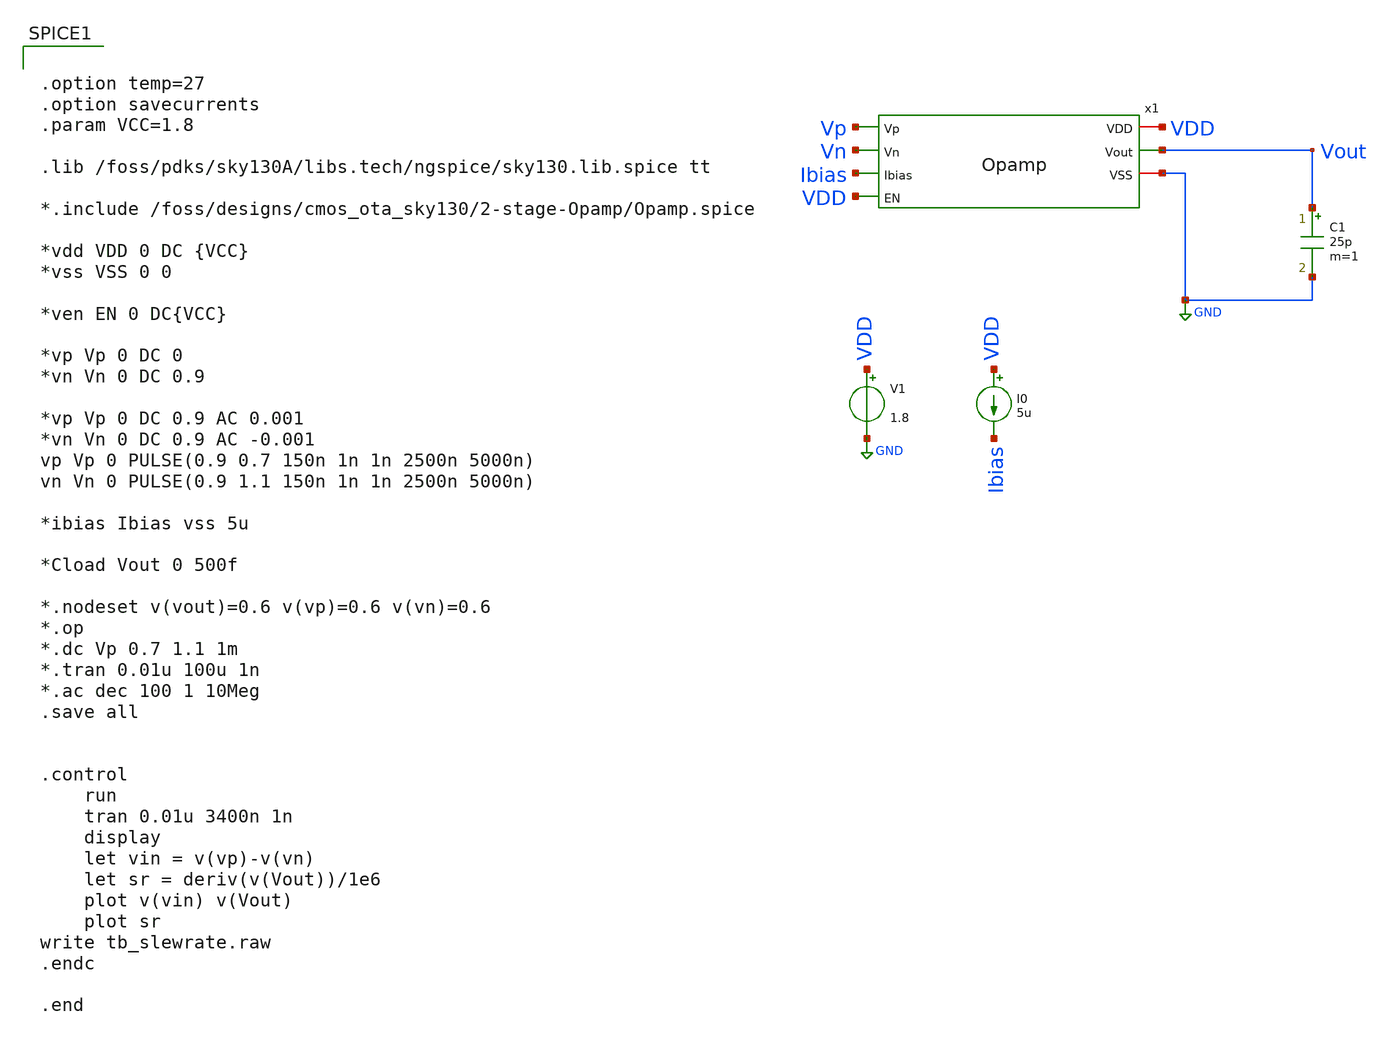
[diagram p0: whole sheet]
** sch_path: xschem/tb_Opamp_slewrate.sch
**.subckt tb_Opamp_slewrate
V1 VDD GND 1.8
C1 Vout GND 25p m=1
I0 VDD Ibias 5u
x1 VDD Vp Vn Vout Ibias GND VDD Opamp
**** begin user architecture code


.option temp=27
.option savecurrents
.param VCC=1.8

.lib /foss/pdks/sky130A/libs.tech/ngspice/sky130.lib.spice tt

*.include /foss/designs/cmos_ota_sky130/2-stage-Opamp/Opamp.spice

*vdd VDD 0 DC {VCC}
*vss VSS 0 0

*ven EN 0 DC{VCC}

*vp Vp 0 DC 0
*vn Vn 0 DC 0.9

*vp Vp 0 DC 0.9 AC 0.001
*vn Vn 0 DC 0.9 AC -0.001
vp Vp 0 PULSE(0.9 0.7 150n 1n 1n 2500n 5000n)
vn Vn 0 PULSE(0.9 1.1 150n 1n 1n 2500n 5000n)

*ibias Ibias vss 5u

*Cload Vout 0 500f

*.nodeset v(vout)=0.6 v(vp)=0.6 v(vn)=0.6
*.op
*.dc Vp 0.7 1.1 1m
*.tran 0.01u 100u 1n
*.ac dec 100 1 10Meg
.save all


.control
	run
	tran 0.01u 3400n 1n
	display
	let vin = v(vp)-v(vn)
	let sr = deriv(v(Vout))/1e6
	plot v(vin) v(Vout)
	plot sr
write tb_slewrate.raw
.endc

.end


**** end user architecture code
**.ends

* expanding   symbol:  /foss/designs/ttsky_se_opamp/xschem/Opamp.sym # of pins=7
** sym_path: xschem/Opamp.sym
** sch_path: xschem/Opamp.sch
.subckt Opamp VDD Vp Vn Vout Ibias VSS EN
*.ipin Vn
*.ipin Ibias
*.ipin Vp
*.ipin EN
*.opin Vout
*.iopin VSS
*.iopin VDD
XM2 Vouts1 Vp Itail GND sky130_fd_pr__nfet_01v8 L=1 W=4 nf=4 ad='int((nf+1)/2) * W/nf * 0.29' as='int((nf+2)/2) * W/nf * 0.29'
+ pd='2*int((nf+1)/2) * (W/nf + 0.29)' ps='2*int((nf+2)/2) * (W/nf + 0.29)' nrd='0.29 / W' nrs='0.29 / W'
+ sa=0 sb=0 sd=0 mult=1 m=1
XM4 Vouts1 net1 VDD VDD sky130_fd_pr__pfet_01v8 L=1 W=4 nf=4 ad='int((nf+1)/2) * W/nf * 0.29' as='int((nf+2)/2) * W/nf * 0.29'
+ pd='2*int((nf+1)/2) * (W/nf + 0.29)' ps='2*int((nf+2)/2) * (W/nf + 0.29)' nrd='0.29 / W' nrs='0.29 / W'
+ sa=0 sb=0 sd=0 mult=2 m=2
XM3 net1 net1 VDD VDD sky130_fd_pr__pfet_01v8 L=1 W=4 nf=4 ad='int((nf+1)/2) * W/nf * 0.29' as='int((nf+2)/2) * W/nf * 0.29'
+ pd='2*int((nf+1)/2) * (W/nf + 0.29)' ps='2*int((nf+2)/2) * (W/nf + 0.29)' nrd='0.29 / W' nrs='0.29 / W'
+ sa=0 sb=0 sd=0 mult=2 m=2
XM1 net1 Vn Itail GND sky130_fd_pr__nfet_01v8 L=1 W=4 nf=4 ad='int((nf+1)/2) * W/nf * 0.29' as='int((nf+2)/2) * W/nf * 0.29'
+ pd='2*int((nf+1)/2) * (W/nf + 0.29)' ps='2*int((nf+2)/2) * (W/nf + 0.29)' nrd='0.29 / W' nrs='0.29 / W'
+ sa=0 sb=0 sd=0 mult=1 m=1
XM6 Vout Vouts1 VDD VDD sky130_fd_pr__pfet_01v8 L=1 W=4 nf=4 ad='int((nf+1)/2) * W/nf * 0.29' as='int((nf+2)/2) * W/nf * 0.29'
+ pd='2*int((nf+1)/2) * (W/nf + 0.29)' ps='2*int((nf+2)/2) * (W/nf + 0.29)' nrd='0.29 / W' nrs='0.29 / W'
+ sa=0 sb=0 sd=0 mult=7 m=7
XM5 Itail Ibias net4 VSS sky130_fd_pr__nfet_01v8 L=1 W=4 nf=4 ad='int((nf+1)/2) * W/nf * 0.29' as='int((nf+2)/2) * W/nf * 0.29'
+ pd='2*int((nf+1)/2) * (W/nf + 0.29)' ps='2*int((nf+2)/2) * (W/nf + 0.29)' nrd='0.29 / W' nrs='0.29 / W'
+ sa=0 sb=0 sd=0 mult=8 m=8
XM7 Vout Ibias net3 VSS sky130_fd_pr__nfet_01v8 L=1 W=4 nf=4 ad='int((nf+1)/2) * W/nf * 0.29' as='int((nf+2)/2) * W/nf * 0.29'
+ pd='2*int((nf+1)/2) * (W/nf + 0.29)' ps='2*int((nf+2)/2) * (W/nf + 0.29)' nrd='0.29 / W' nrs='0.29 / W'
+ sa=0 sb=0 sd=0 mult=11 m=11
XM8 Ibias Ibias net5 VSS sky130_fd_pr__nfet_01v8 L=1 W=4 nf=4 ad='int((nf+1)/2) * W/nf * 0.29' as='int((nf+2)/2) * W/nf * 0.29'
+ pd='2*int((nf+1)/2) * (W/nf + 0.29)' ps='2*int((nf+2)/2) * (W/nf + 0.29)' nrd='0.29 / W' nrs='0.29 / W'
+ sa=0 sb=0 sd=0 mult=1 m=1
XC2 net2 Vout sky130_fd_pr__cap_mim_m3_1 W=30 L=75 MF=2 m=2
Rz net2 Vouts1 sky130_fd_pr__res_generic_l1 W=0.04 L=60 m=1
XM9 net4 EN VSS VSS sky130_fd_pr__nfet_01v8 L=1 W=4 nf=4 ad='int((nf+1)/2) * W/nf * 0.29' as='int((nf+2)/2) * W/nf * 0.29'
+ pd='2*int((nf+1)/2) * (W/nf + 0.29)' ps='2*int((nf+2)/2) * (W/nf + 0.29)' nrd='0.29 / W' nrs='0.29 / W'
+ sa=0 sb=0 sd=0 mult=6 m=6
XM10 net3 EN VSS VSS sky130_fd_pr__nfet_01v8 L=1 W=4 nf=4 ad='int((nf+1)/2) * W/nf * 0.29' as='int((nf+2)/2) * W/nf * 0.29'
+ pd='2*int((nf+1)/2) * (W/nf + 0.29)' ps='2*int((nf+2)/2) * (W/nf + 0.29)' nrd='0.29 / W' nrs='0.29 / W'
+ sa=0 sb=0 sd=0 mult=11 m=11
XM11 net5 EN VSS VSS sky130_fd_pr__nfet_01v8 L=1 W=4 nf=4 ad='int((nf+1)/2) * W/nf * 0.29' as='int((nf+2)/2) * W/nf * 0.29'
+ pd='2*int((nf+1)/2) * (W/nf + 0.29)' ps='2*int((nf+2)/2) * (W/nf + 0.29)' nrd='0.29 / W' nrs='0.29 / W'
+ sa=0 sb=0 sd=0 mult=6 m=6
**** begin user architecture code
"Is Subcircuit" = YES
**** end user architecture code
.ends

.GLOBAL GND
.end
